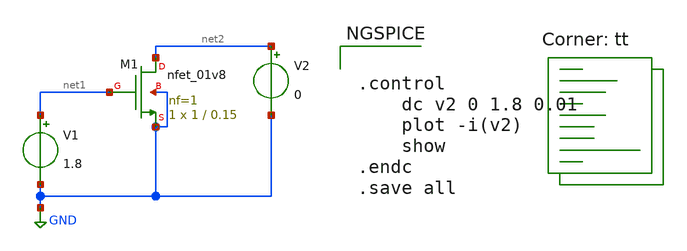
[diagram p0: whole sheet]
** sch_path: cmos_sky130_parameters/nmos_parameters.sch
**.subckt nmos_parameters
V1 net1 GND 1.8
XM1 net2 net1 GND GND sky130_fd_pr__nfet_01v8 L=0.15 W=1 nf=1 ad='int((nf+1)/2) * W/nf * 0.29' as='int((nf+2)/2) * W/nf * 0.29'
+ pd='2*int((nf+1)/2) * (W/nf + 0.29)' ps='2*int((nf+2)/2) * (W/nf + 0.29)' nrd='0.29 / W' nrs='0.29 / W'
+ sa=0 sb=0 sd=0 mult=1 m=1
V2 net2 GND 0
**** begin user architecture code


.control
	dc v2 0 1.8 0.01
	plot -i(v2)
	show
.endc
.save all


.lib $::SKYWATER_MODELS/sky130.lib.spice tt
**** end user architecture code
**.ends
.GLOBAL GND
.end
